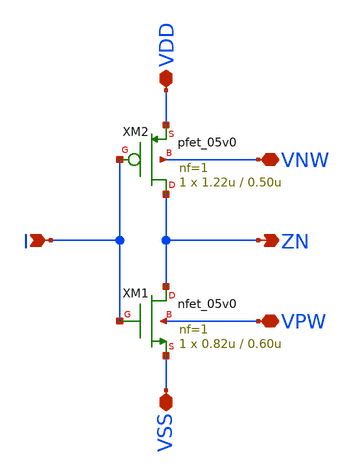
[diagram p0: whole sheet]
** sch_path: _tests/23/gf180mcuD/inv.sch
**.subckt inv I ZN VDD VSS VNW VPW
*.ipin I
*.opin ZN
*.iopin VDD
*.iopin VSS
*.iopin VNW
*.iopin VPW
XM1 ZN I VSS VPW nfet_05v0 L=0.60u W=0.82u nf=1 ad='int((nf+1)/2) * W/nf * 0.18u' as='int((nf+2)/2) * W/nf * 0.18u'
+ pd='2*int((nf+1)/2) * (W/nf + 0.18u)' ps='2*int((nf+2)/2) * (W/nf + 0.18u)' nrd='0.18u / W' nrs='0.18u / W'
+ sa=0 sb=0 sd=0 m=1
XM2 ZN I VDD VNW pfet_05v0 L=0.50u W=1.22u nf=1 ad='int((nf+1)/2) * W/nf * 0.18u' as='int((nf+2)/2) * W/nf * 0.18u'
+ pd='2*int((nf+1)/2) * (W/nf + 0.18u)' ps='2*int((nf+2)/2) * (W/nf + 0.18u)' nrd='0.18u / W' nrs='0.18u / W'
+ sa=0 sb=0 sd=0 m=1 par=1
**.ends
.end
